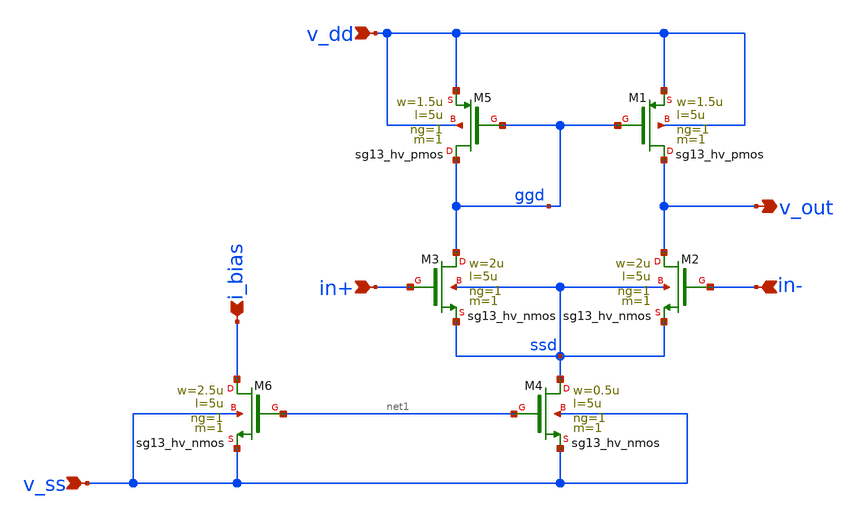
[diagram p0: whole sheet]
** sch_path: 3_Real_Cir/self_build_opamp.sch
**.subckt self_build_opamp in+ in- v_ss v_dd i_bias v_out
*.ipin in+
*.ipin in-
*.ipin v_ss
*.ipin v_dd
*.ipin i_bias
*.opin v_out
XM3 ggd in+ ssd ssd sg13_hv_nmos w=2u l=5u ng=1 m=1 mm_ok=1
XM2 v_out in- ssd ssd sg13_hv_nmos w=2u l=5u ng=1 m=1 mm_ok=1
XM4 ssd net1 v_ss v_ss sg13_hv_nmos w=0.5u l=5u ng=1 m=1 mm_ok=1
XM5 ggd ggd v_dd v_dd sg13_hv_pmos w=1.5u l=5u ng=1 m=1 mm_ok=1
XM1 v_out ggd v_dd v_dd sg13_hv_pmos w=1.5u l=5u ng=1 m=1 mm_ok=1
XM6 i_bias net1 v_ss v_ss sg13_hv_nmos w=2.5u l=5u ng=1 m=1 mm_ok=1
**.ends
.end
